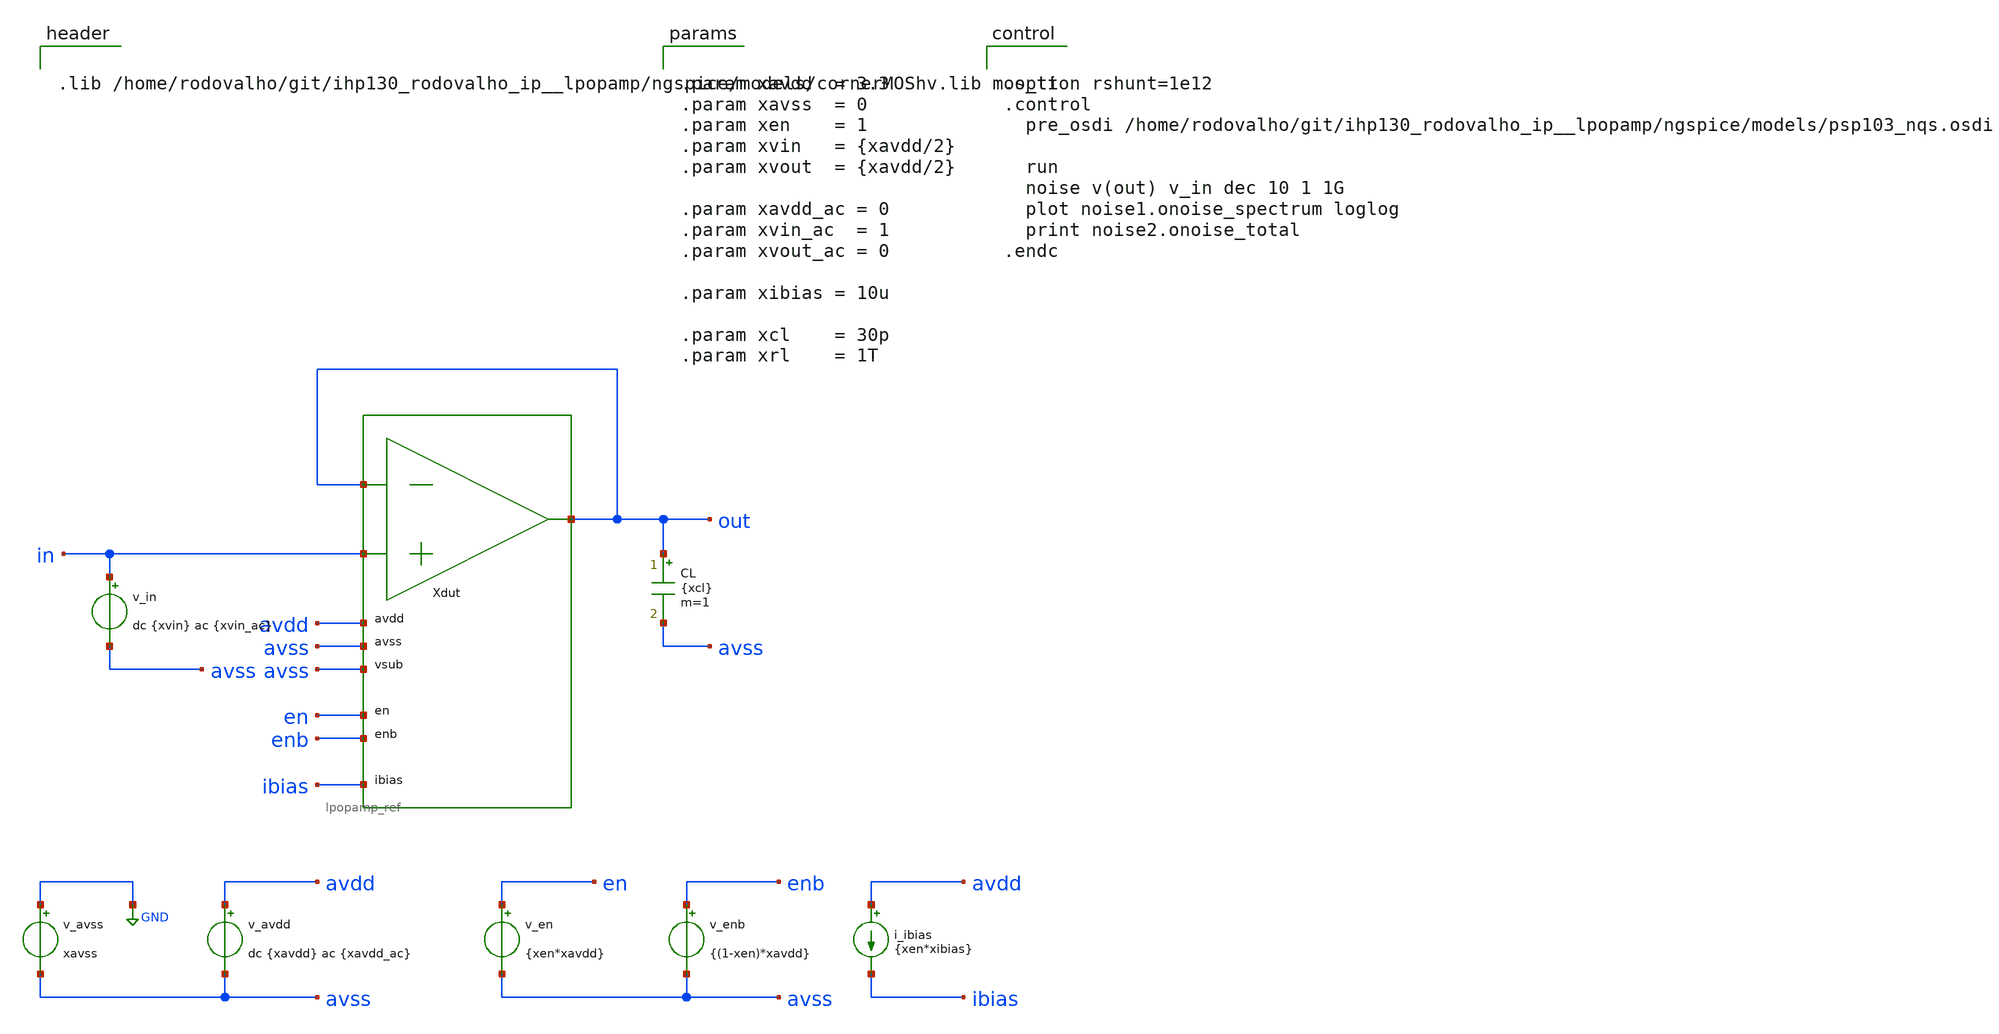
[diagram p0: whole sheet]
** sch_path: xschem/tb_lpopamp_buf_noise.sch
**.subckt tb_lpopamp_buf_noise
Xdut out in out avdd avss avss en enb ibias lpopamp_ref
v_avss GND avss xavss
v_avdd avdd avss dc {xavdd} ac {xavdd_ac}
v_in in avss dc {xvin} ac {xvin_ac}
v_en en avss {xen*xavdd}
v_enb enb avss {(1-xen)*xavdd}
i_ibias avdd ibias {xen*xibias}
CL out avss {xcl} m=1
**** begin user architecture code


.lib /home/rodovalho/git/ihp130_rodovalho_ip__lpopamp/ngspice/models/cornerMOShv.lib mos_tt




.option rshunt=1e12
.control
  pre_osdi /home/rodovalho/git/ihp130_rodovalho_ip__lpopamp/ngspice/models/psp103_nqs.osdi

  run
  noise v(out) v_in dec 10 1 1G
  plot noise1.onoise_spectrum loglog
  print noise2.onoise_total
.endc




.param xavdd  = 3.3
.param xavss  = 0
.param xen    = 1
.param xvin   = {xavdd/2}
.param xvout  = {xavdd/2}

.param xavdd_ac = 0
.param xvin_ac  = 1
.param xvout_ac = 0

.param xibias = 10u

.param xcl    = 30p
.param xrl    = 1T


**** end user architecture code
**.ends
.GLOBAL GND
.end
